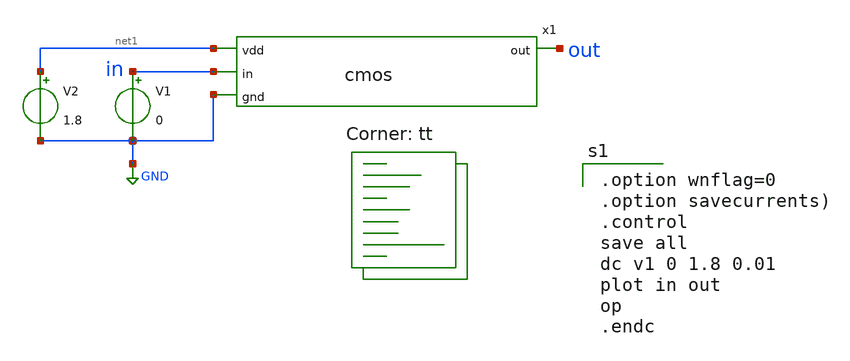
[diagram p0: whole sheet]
** sch_path: CMOS inverter/cmos_tb.sch
**.subckt cmos_tb
x1 net1 in out GND cmos
V1 in GND 0
V2 net1 GND 1.8
**** begin user architecture code
.lib $::SKYWATER_MODELS/sky130.lib.spice tt

.option wnflag=0
.option savecurrents)
.control
save all
dc v1 0 1.8 0.01
plot in out
op
.endc

**** end user architecture code
**.ends

* expanding   symbol:  cmos.sym # of pins=4
** sym_path: CMOS inverter/cmos.sym
** sch_path: CMOS inverter/cmos.sch
.subckt cmos vdd in out gnd
*.ipin vdd
*.ipin in
*.ipin gnd
*.opin out
XM1 out in gnd gnd sky130_fd_pr__nfet_01v8 L=0.15 W=1 nf=1 ad='int((nf+1)/2) * W/nf * 0.29' as='int((nf+2)/2) * W/nf * 0.29'
+ pd='2*int((nf+1)/2) * (W/nf + 0.29)' ps='2*int((nf+2)/2) * (W/nf + 0.29)' nrd='0.29 / W' nrs='0.29 / W'
+ sa=0 sb=0 sd=0 mult=1 m=1
XM2 out in vdd vdd sky130_fd_pr__pfet_01v8 L=0.15 W=1 nf=1 ad='int((nf+1)/2) * W/nf * 0.29' as='int((nf+2)/2) * W/nf * 0.29'
+ pd='2*int((nf+1)/2) * (W/nf + 0.29)' ps='2*int((nf+2)/2) * (W/nf + 0.29)' nrd='0.29 / W' nrs='0.29 / W'
+ sa=0 sb=0 sd=0 mult=1 m=1
.ends

.GLOBAL GND
.end
